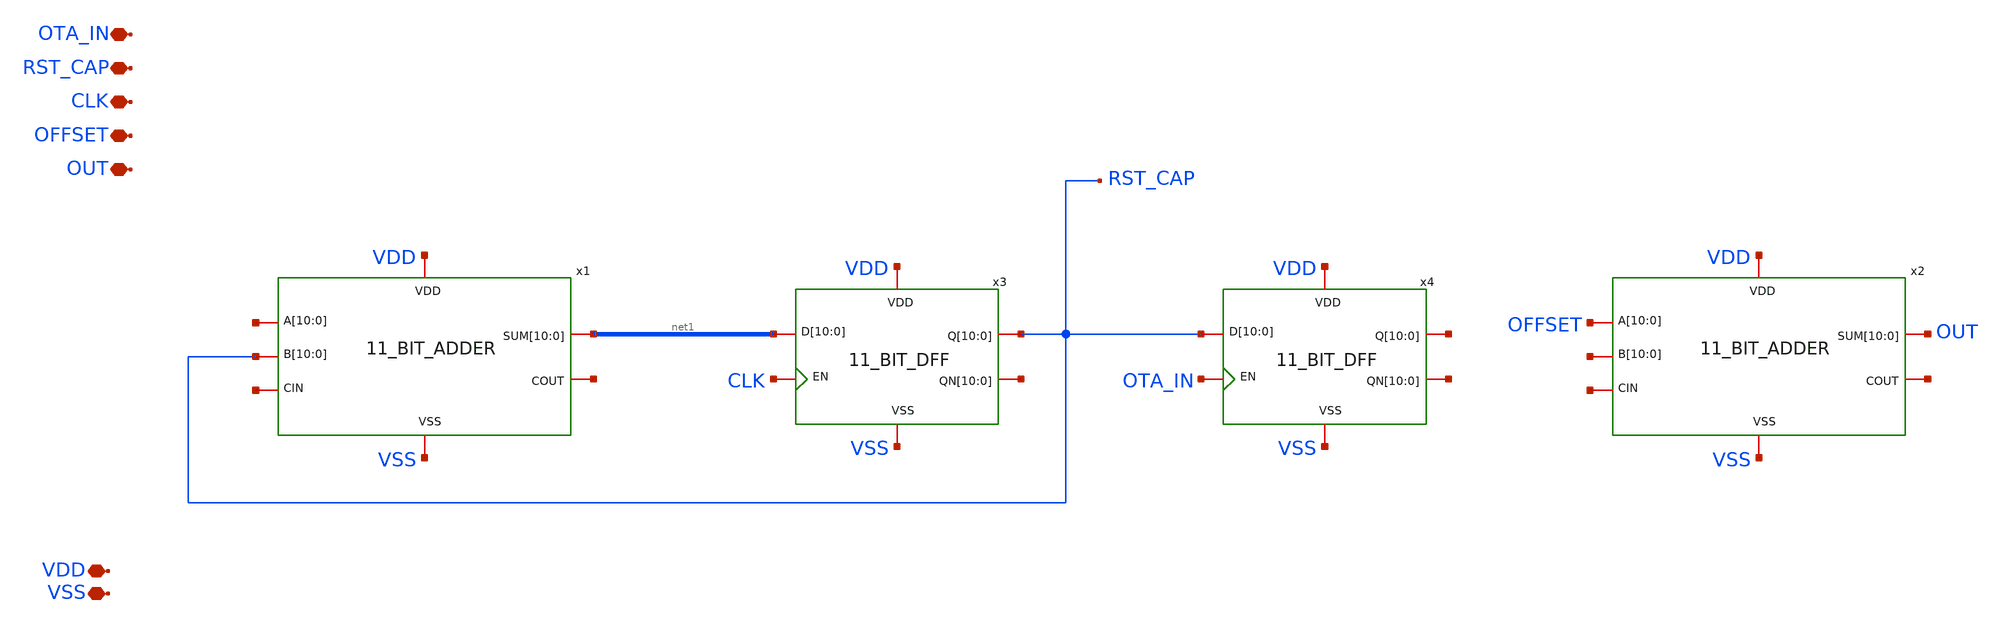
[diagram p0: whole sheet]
** sch_path: design/CNR_GR03_SKY130NM/MILESTONE3.sch
**.subckt MILESTONE3 VDD VSS OTA_IN RST_CAP CLK OFFSET OUT
*.iopin VDD
*.iopin VSS
*.iopin OTA_IN
*.iopin RST_CAP
*.iopin CLK
*.iopin OFFSET
*.iopin OUT
x1 net1[10] net1[9] net1[8] net1[7] net1[6] net1[5] net1[4] net1[3] net1[2] net1[1] net1[0] net2[10]
+ net2[9] net2[8] net2[7] net2[6] net2[5] net2[4] net2[3] net2[2] net2[1] net2[0] RST_CAP RST_CAP RST_CAP
+ RST_CAP RST_CAP RST_CAP RST_CAP RST_CAP RST_CAP RST_CAP RST_CAP net3 net4 VDD VSS 11_BIT_ADDER
x2 OUT OUT OUT OUT OUT OUT OUT OUT OUT OUT OUT OFFSET OFFSET OFFSET OFFSET OFFSET OFFSET OFFSET
+ OFFSET OFFSET OFFSET OFFSET net5[10] net5[9] net5[8] net5[7] net5[6] net5[5] net5[4] net5[3] net5[2]
+ net5[1] net5[0] net6 net7 VDD VSS 11_BIT_ADDER
x3 VDD VSS net1[10] net1[9] net1[8] net1[7] net1[6] net1[5] net1[4] net1[3] net1[2] net1[1] net1[0]
+ RST_CAP RST_CAP RST_CAP RST_CAP RST_CAP RST_CAP RST_CAP RST_CAP RST_CAP RST_CAP RST_CAP net8[10] net8[9]
+ net8[8] net8[7] net8[6] net8[5] net8[4] net8[3] net8[2] net8[1] net8[0] CLK 11_BIT_DFF
x4 VDD VSS RST_CAP RST_CAP RST_CAP RST_CAP RST_CAP RST_CAP RST_CAP RST_CAP RST_CAP RST_CAP RST_CAP
+ net9[10] net9[9] net9[8] net9[7] net9[6] net9[5] net9[4] net9[3] net9[2] net9[1] net9[0] net10[10] net10[9]
+ net10[8] net10[7] net10[6] net10[5] net10[4] net10[3] net10[2] net10[1] net10[0] OTA_IN 11_BIT_DFF
**.ends
.end
